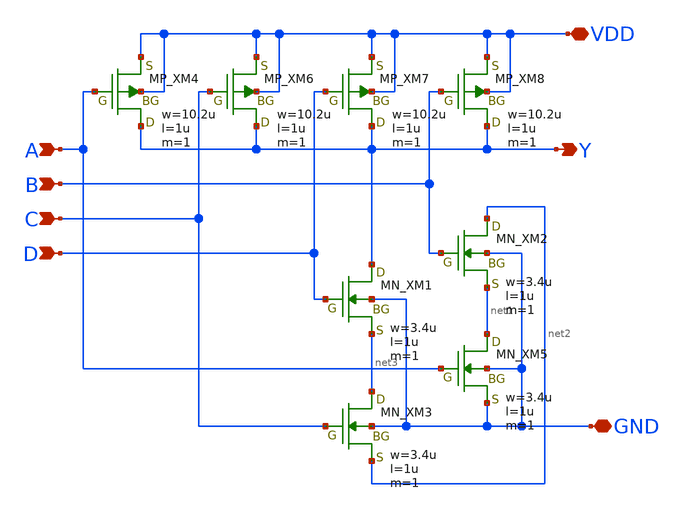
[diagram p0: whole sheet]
** sch_path: openIP62_rev1.0/IP62/Technology/tech/symbols/Xschem/IP62_5_stdcell/NAND4.sch
**.subckt NAND4 B A Y GND VDD D C
*.ipin B
*.ipin A
*.opin Y
*.iopin GND
*.iopin VDD
*.ipin D
*.ipin C
XM4 Y A VDD VDD PMOS w=10.2u l=1u as=0 ad=0 ps=0 pd=0 nrd=0 nrs=0 m=1
XM6 Y C VDD VDD PMOS w=10.2u l=1u as=0 ad=0 ps=0 pd=0 nrd=0 nrs=0 m=1
XM7 Y D VDD VDD PMOS w=10.2u l=1u as=0 ad=0 ps=0 pd=0 nrd=0 nrs=0 m=1
XM8 Y B VDD VDD PMOS w=10.2u l=1u as=0 ad=0 ps=0 pd=0 nrd=0 nrs=0 m=1
XM1 Y D net3 GND NMOS w=3.4u l=1u as=0 ad=0 ps=0 pd=0 nrd=0 nrs=0 m=1
XM2 net2 B net1 GND NMOS w=3.4u l=1u as=0 ad=0 ps=0 pd=0 nrd=0 nrs=0 m=1
XM3 net3 C net2 GND NMOS w=3.4u l=1u as=0 ad=0 ps=0 pd=0 nrd=0 nrs=0 m=1
XM5 net1 A GND GND NMOS w=3.4u l=1u as=0 ad=0 ps=0 pd=0 nrd=0 nrs=0 m=1
**.ends
.end
